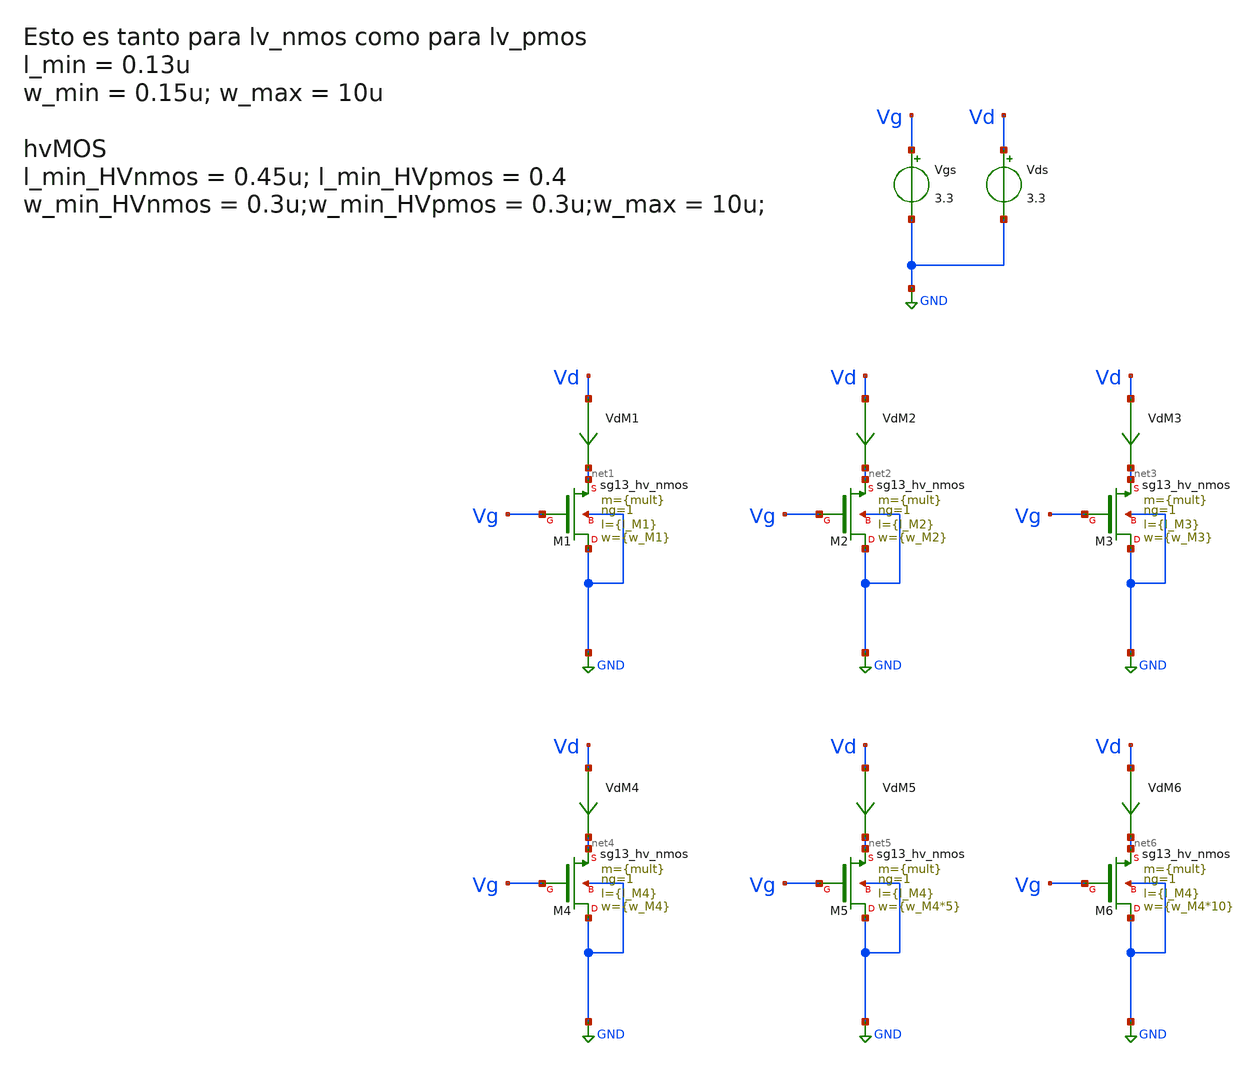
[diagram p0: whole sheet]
** sch_path: ChipUSM_AnalogTrack24/TestBenchs/TB_hvNMOS_charact.sch
**.subckt TB_hvNMOS_charact
XM1 GND Vg net1 GND sg13_hv_nmos w={w_M1} l={l_M1} ng=1 m={mult} mm_ok=1
Vgs Vg GND 3.3
Vds Vd GND 3.3
VdM1 Vd net1 0
.save i(vdm1)
XM2 GND Vg net2 GND sg13_hv_nmos w={w_M2} l={l_M2} ng=1 m={mult} mm_ok=1
VdM2 Vd net2 0
.save i(vdm2)
XM3 GND Vg net3 GND sg13_hv_nmos w={w_M3} l={l_M3} ng=1 m={mult} mm_ok=1
VdM3 Vd net3 0
.save i(vdm3)
XM4 GND Vg net4 GND sg13_hv_nmos w={w_M4} l={l_M4} ng=1 m={mult} mm_ok=1
VdM4 Vd net4 0
.save i(vdm4)
XM5 GND Vg net5 GND sg13_hv_nmos w={w_M4*5} l={l_M4} ng=1 m={mult} mm_ok=1
VdM5 Vd net5 0
.save i(vdm5)
XM6 GND Vg net6 GND sg13_hv_nmos w={w_M4*10} l={l_M4} ng=1 m={mult} mm_ok=1
VdM6 Vd net6 0
.save i(vdm6)
**** begin user architecture code


.param temp=27
.param mult = 1

.param w_M1 =10u
.param l_M1 =0.45u

.param w_M2 =10u
.param l_M2 =0.55u

.param w_M3 =10u
.param l_M3 =0.65u

.param w_M4 = 1u
.param l_M4 = 1u

.save all
* + @M.XM1.m1[id]  @n.xm1.nsg13_hv_nmos[vth]  @n.xm1.nsg13_hv_nmos[gds]  @n.xm2.nsg13_hv_nmos[vth]
*+  @n.xm2.nsg13_hv_nmos[gds]  @n.xm3.nsg13_hv_nmos[vth]  @n.xm3.nsg13_hv_nmos[gds]  @n.xm4.nsg13_hv_nmos[vth]
*+  @n.xm4.nsg13_hv_nmos[gds]  @n.xm5.nsg13_hv_nmos[vth]  @n.xm5.nsg13_hv_nmos[gds]  @n.xm6.nsg13_hv_nmos[vth]
*+  @n.xm6.nsg13_hv_nmos[gds]  @n.xm1.nsg13_hv_nmos[ad]

.control
*dc Vds 0 3 0.01 Vgs 0.5 3 0.5
dc Vds 0 3.3 0.01
*dc Vds 0 0.5 0.01
*dc Vds 0 0.5 0.01 temp 0 27 1
write dc_hv_nmos.raw
let G_M1 = @n.xm1.nsg13_hv_nmos[gds]
let G_M2 = @n.xm2.nsg13_hv_nmos[gds]
let G_M3 = @n.xm3.nsg13_hv_nmos[gds]
let G_M4 = @n.xm4.nsg13_hv_nmos[gds]
let G_M5 = @n.xm5.nsg13_hv_nmos[gds]
let G_M6 = @n.xm6.nsg13_hv_nmos[gds]
let Ron_M1 = 1/G_M1
let Ron_M2 = 1/G_M2
let Ron_M3 = 1/G_M3
let Ron_M4 = 1/G_M4
let Ron_M5 = 1/G_M5
let Ron_M6 = 1/G_M6
let Vds = v(Vd)

let Vth_M1 = @n.xm1.nsg13_hv_nmos[vth]
let Vth_M2 = @n.xm2.nsg13_hv_nmos[vth]
let Vth_M3 = @n.xm3.nsg13_hv_nmos[vth]

let Id_M1 = i(VdM1)
plot i(VdM1) i(VdM2) i(VdM3) vs Vds
plot Ron_M1 Ron_M2 Ron_M3 vs Vds
plot i(VdM4) i(VdM5) i(VdM6) vs Vds
plot Ron_M4 Ron_M5 Ron_M6 vs Vds
plot Vth_M1 Vth_M2 Vth_M3 vs Vds
*print @n.xm1.nsg13_hv_nmos[vth] @n.xm2.nsg13_hv_nmos[vth] Vth_M1
*print @n.xm2.nsg13_hv_nmos[vth]
write test_nmos.raw




.endc





.lib cornerMOShv.lib mos_tt

**** end user architecture code
**.ends
.GLOBAL GND
.end
